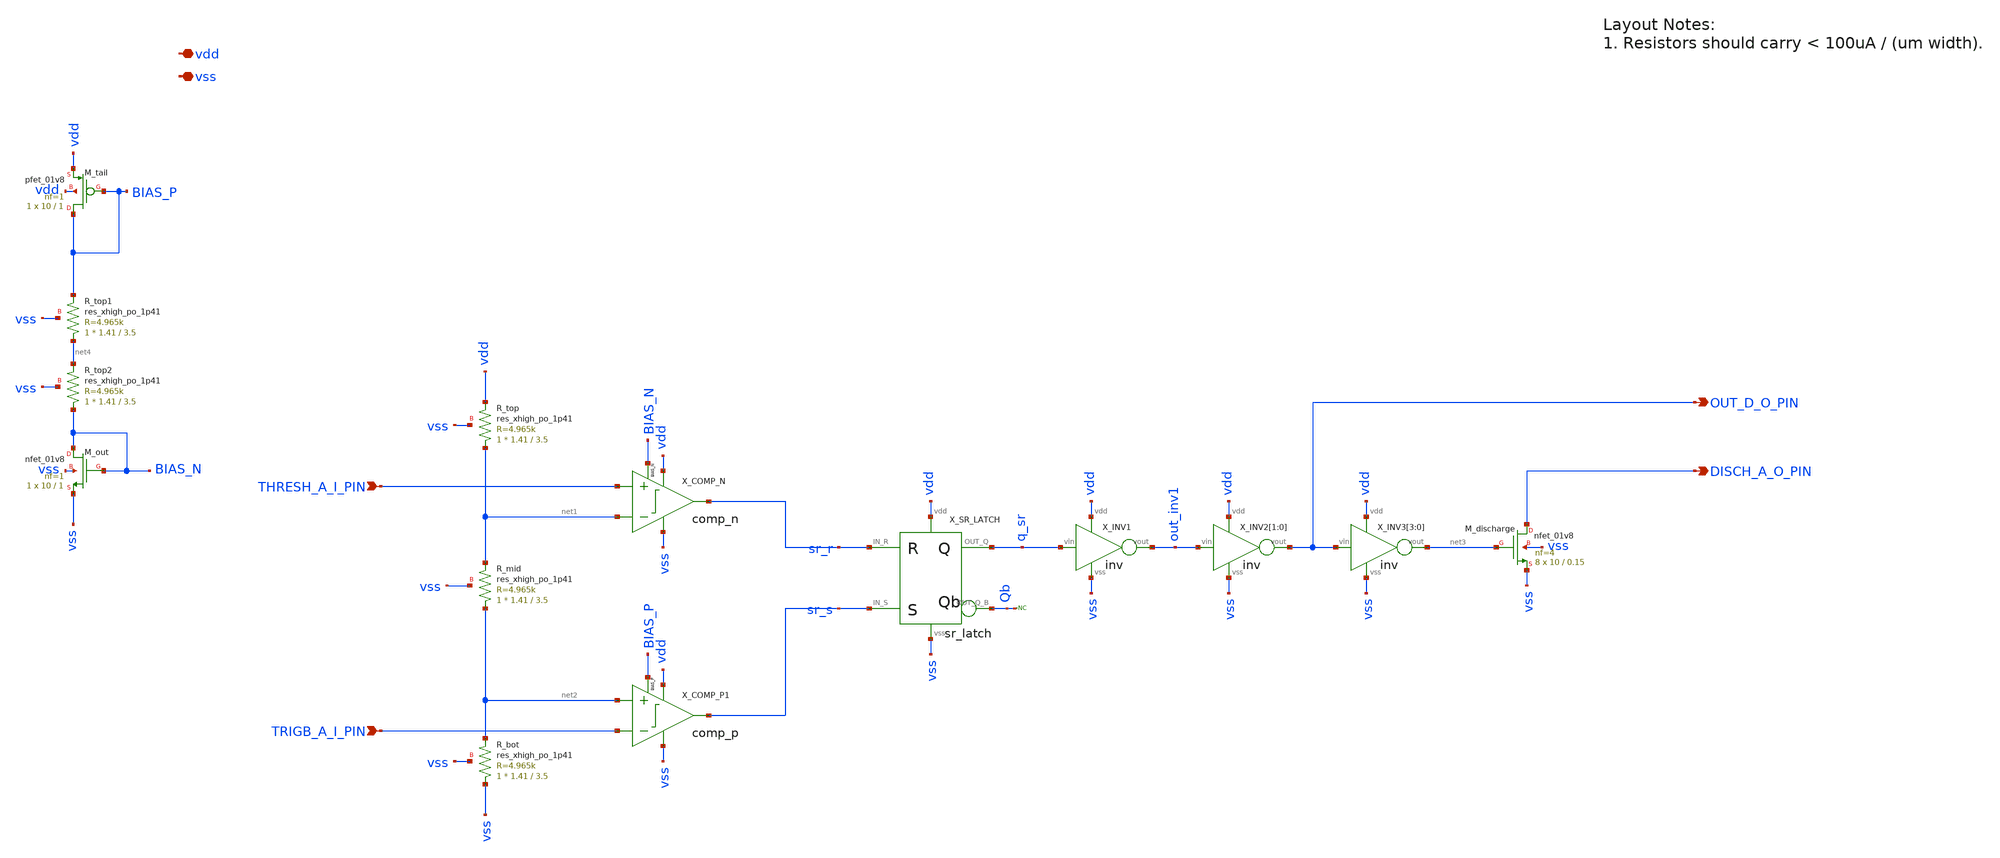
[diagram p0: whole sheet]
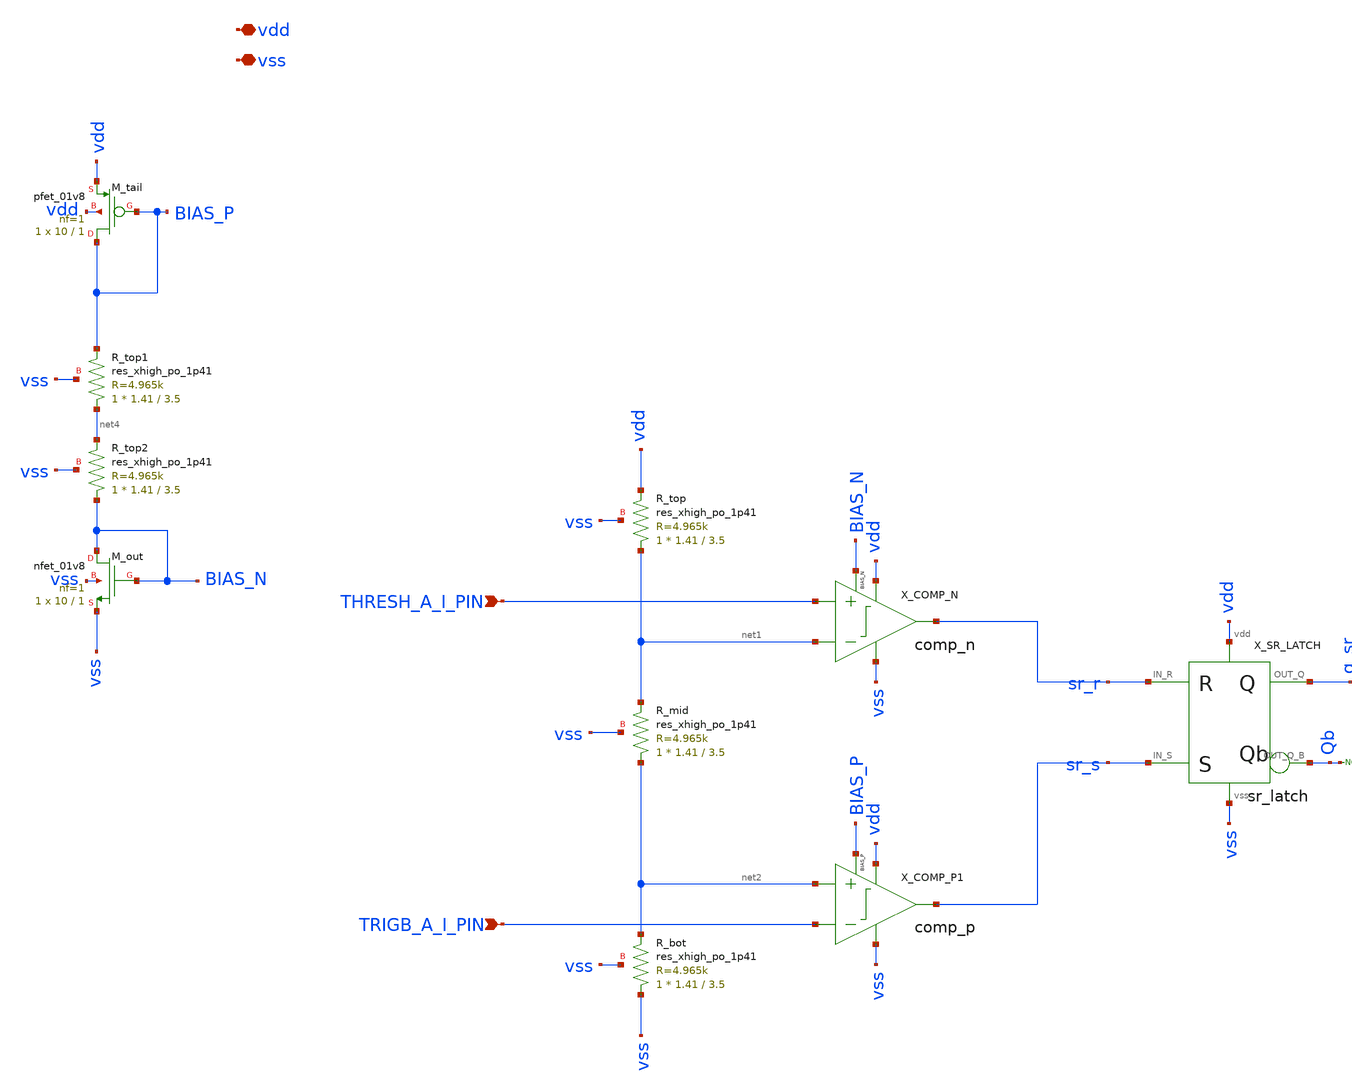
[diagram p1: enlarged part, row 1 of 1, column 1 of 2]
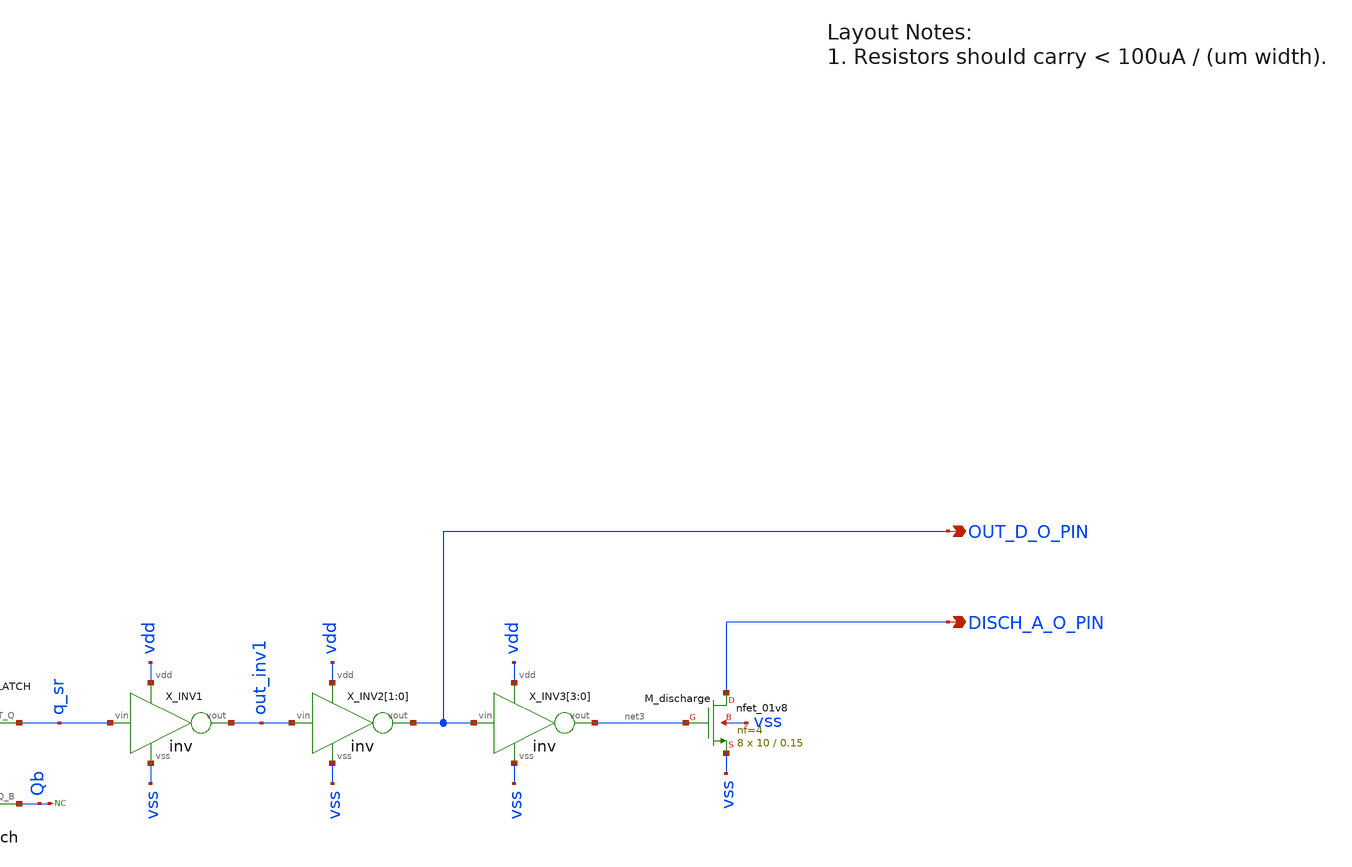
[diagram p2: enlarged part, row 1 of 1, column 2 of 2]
** sch_path: xsch/ip/timer_core.sch
**.subckt timer_core THRESH_A_I_PIN TRIGB_A_I_PIN OUT_D_O_PIN vdd vss DISCH_A_O_PIN
*.ipin THRESH_A_I_PIN
*.ipin TRIGB_A_I_PIN
*.opin OUT_D_O_PIN
*.iopin vdd
*.iopin vss
*.opin DISCH_A_O_PIN
XR_top net1 vdd vss sky130_fd_pr__res_xhigh_po_1p41 L=3.5 mult=1 m=1
XR_mid net2 net1 vss sky130_fd_pr__res_xhigh_po_1p41 L=3.5 mult=1 m=1
XR_bot vss net2 vss sky130_fd_pr__res_xhigh_po_1p41 L=3.5 mult=1 m=1
X_SR_LATCH sr_s Qb vdd vss sr_r q_sr sr_latch
XM_discharge DISCH_A_O_PIN net3 vss vss sky130_fd_pr__nfet_01v8 L=0.15 W=10 nf=4 ad='int((nf+1)/2) * W/nf * 0.29'
+ as='int((nf+2)/2) * W/nf * 0.29' pd='2*int((nf+1)/2) * (W/nf + 0.29)' ps='2*int((nf+2)/2) * (W/nf + 0.29)'
+ nrd='0.29 / W' nrs='0.29 / W' sa=0 sb=0 sd=0 mult=8 m=8
X_INV1 q_sr out_inv1 vdd vss inv
X_INV2[1] out_inv1 OUT_D_O_PIN vdd vss inv
X_INV2[0] out_inv1 OUT_D_O_PIN vdd vss inv
X_INV3[3] OUT_D_O_PIN net3 vdd vss inv
X_INV3[2] OUT_D_O_PIN net3 vdd vss inv
X_INV3[1] OUT_D_O_PIN net3 vdd vss inv
X_INV3[0] OUT_D_O_PIN net3 vdd vss inv
X_COMP_N THRESH_A_I_PIN sr_r vdd vss net1 BIAS_N comp_n
* noconn Qb
XM_tail BIAS_P BIAS_P vdd vdd sky130_fd_pr__pfet_01v8 L=1 W=10 nf=1 ad='int((nf+1)/2) * W/nf * 0.29'
+ as='int((nf+2)/2) * W/nf * 0.29' pd='2*int((nf+1)/2) * (W/nf + 0.29)' ps='2*int((nf+2)/2) * (W/nf + 0.29)'
+ nrd='0.29 / W' nrs='0.29 / W' sa=0 sb=0 sd=0 mult=1 m=1
XR_top1 net4 BIAS_P vss sky130_fd_pr__res_xhigh_po_1p41 L=3.5 mult=1 m=1
XR_top2 BIAS_N net4 vss sky130_fd_pr__res_xhigh_po_1p41 L=3.5 mult=1 m=1
X_COMP_P1 net2 sr_s vdd vss TRIGB_A_I_PIN BIAS_P comp_p
XM_out BIAS_N BIAS_N vss vss sky130_fd_pr__nfet_01v8 L=1 W=10 nf=1 ad='int((1 + 1)/2) * 10 / 1 * 0.29'
+ as='int((1 + 2)/2) * 10 / 1 * 0.29' pd='2*int((1 + 1)/2) * (10 / 1 + 0.29)' ps='2*int((1 + 2)/2) * (10 / 1 + 0.29)'
+ nrd='0.29 / 10 ' nrs='0.29 / 10 ' sa=0 sb=0 sd=0 mult=1 m=1
**.ends
.end
